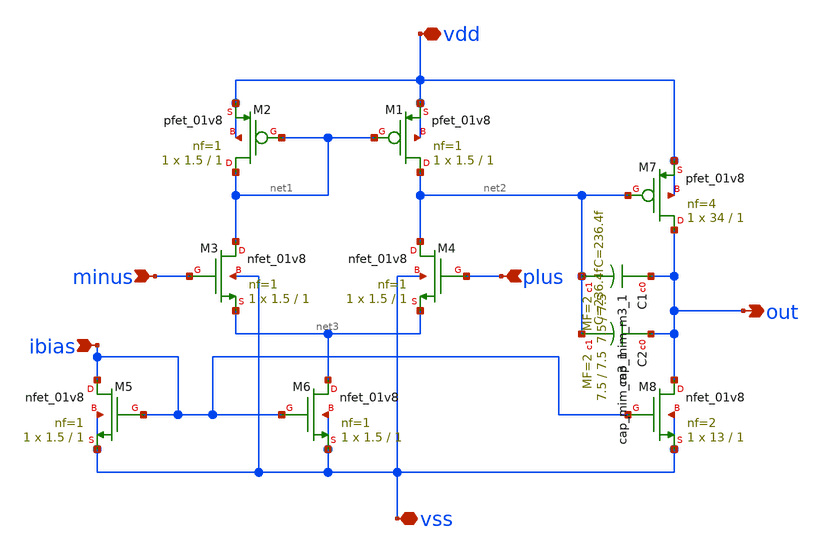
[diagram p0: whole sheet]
** sch_path: 2OTA.sch
**.subckt 2OTA ibias minus plus vdd vss out
*.ipin ibias
*.ipin minus
*.ipin plus
*.iopin vdd
*.iopin vss
*.opin out
XM1 net2 net1 vdd vdd sky130_fd_pr__pfet_01v8 L=1 W=1.5 nf=1 ad='int((1 + 1)/2) * 1.5 / 1 * 0.29' as='int((1 + 2)/2) * 1.5 / 1 * 0.29'
+ pd='2*int((1 + 1)/2) * (1.5 / 1 + 0.29)' ps='2*int((1 + 2)/2) * (1.5 / 1 + 0.29)' nrd='0.29 / 1.5 ' nrs='0.29 / 1.5 '
+ sa=0 sb=0 sd=0 mult=1 m=1
XM2 net1 net1 vdd vdd sky130_fd_pr__pfet_01v8 L=1 W=1.5 nf=1 ad='int((1 + 1)/2) * 1.5 / 1 * 0.29' as='int((1 + 2)/2) * 1.5 / 1 * 0.29'
+ pd='2*int((1 + 1)/2) * (1.5 / 1 + 0.29)' ps='2*int((1 + 2)/2) * (1.5 / 1 + 0.29)' nrd='0.29 / 1.5 ' nrs='0.29 / 1.5 '
+ sa=0 sb=0 sd=0 mult=1 m=1
XM3 net1 minus net3 vss sky130_fd_pr__nfet_01v8 L=1 W=1.5 nf=1 ad='int((1 + 1)/2) * 1.5 / 1 * 0.29' as='int((1 + 2)/2) * 1.5 / 1 * 0.29'
+ pd='2*int((1 + 1)/2) * (1.5 / 1 + 0.29)' ps='2*int((1 + 2)/2) * (1.5 / 1 + 0.29)' nrd='0.29 / 1.5 ' nrs='0.29 / 1.5 '
+ sa=0 sb=0 sd=0 mult=1 m=1
XM4 net2 plus net3 vss sky130_fd_pr__nfet_01v8 L=1 W=1.5 nf=1 ad='int((1 + 1)/2) * 1.5 / 1 * 0.29' as='int((1 + 2)/2) * 1.5 / 1 * 0.29'
+ pd='2*int((1 + 1)/2) * (1.5 / 1 + 0.29)' ps='2*int((1 + 2)/2) * (1.5 / 1 + 0.29)' nrd='0.29 / 1.5 ' nrs='0.29 / 1.5 '
+ sa=0 sb=0 sd=0 mult=1 m=1
XM5 ibias ibias vss vss sky130_fd_pr__nfet_01v8 L=1 W=1.5 nf=1 ad='int((1 + 1)/2) * 1.5 / 1 * 0.29' as='int((1 + 2)/2) * 1.5 / 1 * 0.29'
+ pd='2*int((1 + 1)/2) * (1.5 / 1 + 0.29)' ps='2*int((1 + 2)/2) * (1.5 / 1 + 0.29)' nrd='0.29 / 1.5 ' nrs='0.29 / 1.5 '
+ sa=0 sb=0 sd=0 mult=1 m=1
XM6 net3 ibias vss vss sky130_fd_pr__nfet_01v8 L=1 W=1.5 nf=1 ad='int((1 + 1)/2) * 1.5 / 1 * 0.29' as='int((1 + 2)/2) * 1.5 / 1 * 0.29'
+ pd='2*int((1 + 1)/2) * (1.5 / 1 + 0.29)' ps='2*int((1 + 2)/2) * (1.5 / 1 + 0.29)' nrd='0.29 / 1.5 ' nrs='0.29 / 1.5 '
+ sa=0 sb=0 sd=0 mult=1 m=1
XM7 out net2 vdd vdd sky130_fd_pr__pfet_01v8 L=1 W=34 nf=4 ad='int((4 + 1)/2) * 34 / 4 * 0.29' as='int((4 + 2)/2) * 34 / 4 * 0.29'
+ pd='2*int((4 + 1)/2) * (34 / 4 + 0.29)' ps='2*int((4 + 2)/2) * (34 / 4 + 0.29)' nrd='0.29 / 34 ' nrs='0.29 / 34 '
+ sa=0 sb=0 sd=0 mult=1 m=1
XM8 out ibias vss vss sky130_fd_pr__nfet_01v8 L=1 W=13 nf=2 ad='int((2 + 1)/2) * 13 / 2 * 0.29' as='int((2 + 2)/2) * 13 / 2 * 0.29'
+ pd='2*int((2 + 1)/2) * (13 / 2 + 0.29)' ps='2*int((2 + 2)/2) * (13 / 2 + 0.29)' nrd='0.29 / 13 ' nrs='0.29 / 13 '
+ sa=0 sb=0 sd=0 mult=1 m=1
XC1 out net2 sky130_fd_pr__cap_mim_m3_1 W=7.5 L=7.5 MF=2 m=2
XC2 out net2 sky130_fd_pr__cap_mim_m3_1 W=7.5 L=7.5 MF=2 m=2
**.ends
.end
